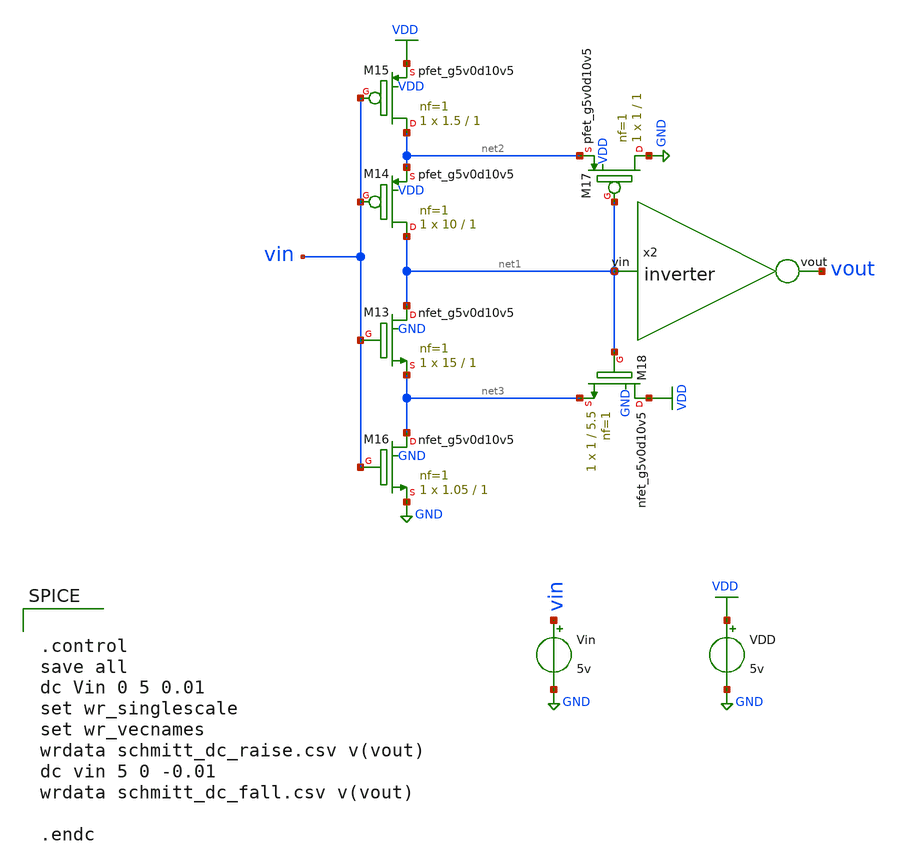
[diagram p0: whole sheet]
** sch_path: schematics/schmitt_trigger_tb.sch
**.subckt schmitt_trigger_tb
VDD VDD GND 5v
Vin vin GND 5v
XM13 net1 vin net3 GND sky130_fd_pr__nfet_g5v0d10v5 L=1 W=15 nf=1 ad='int((nf+1)/2) * W/nf * 0.29' as='int((nf+2)/2) * W/nf * 0.29'
+ pd='2*int((nf+1)/2) * (W/nf + 0.29)' ps='2*int((nf+2)/2) * (W/nf + 0.29)' nrd='0.29 / W' nrs='0.29 / W'
+ sa=0 sb=0 sd=0 mult=1 m=1
XM14 net1 vin net2 VDD sky130_fd_pr__pfet_g5v0d10v5 L=1 W=10 nf=1 ad='int((nf+1)/2) * W/nf * 0.29' as='int((nf+2)/2) * W/nf * 0.29'
+ pd='2*int((nf+1)/2) * (W/nf + 0.29)' ps='2*int((nf+2)/2) * (W/nf + 0.29)' nrd='0.29 / W' nrs='0.29 / W'
+ sa=0 sb=0 sd=0 mult=1 m=1
XM15 net2 vin VDD VDD sky130_fd_pr__pfet_g5v0d10v5 L=1 W=1.5 nf=1 ad='int((nf+1)/2) * W/nf * 0.29' as='int((nf+2)/2) * W/nf * 0.29'
+ pd='2*int((nf+1)/2) * (W/nf + 0.29)' ps='2*int((nf+2)/2) * (W/nf + 0.29)' nrd='0.29 / W' nrs='0.29 / W'
+ sa=0 sb=0 sd=0 mult=1 m=1
XM16 net3 vin GND GND sky130_fd_pr__nfet_g5v0d10v5 L=1 W=1.05 nf=1 ad='int((nf+1)/2) * W/nf * 0.29' as='int((nf+2)/2) * W/nf * 0.29'
+ pd='2*int((nf+1)/2) * (W/nf + 0.29)' ps='2*int((nf+2)/2) * (W/nf + 0.29)' nrd='0.29 / W' nrs='0.29 / W'
+ sa=0 sb=0 sd=0 mult=1 m=1
XM17 GND net1 net2 VDD sky130_fd_pr__pfet_g5v0d10v5 L=1 W=1 nf=1 ad='int((nf+1)/2) * W/nf * 0.29' as='int((nf+2)/2) * W/nf * 0.29'
+ pd='2*int((nf+1)/2) * (W/nf + 0.29)' ps='2*int((nf+2)/2) * (W/nf + 0.29)' nrd='0.29 / W' nrs='0.29 / W'
+ sa=0 sb=0 sd=0 mult=1 m=1
XM18 VDD net1 net3 GND sky130_fd_pr__nfet_g5v0d10v5 L=5.5 W=1 nf=1 ad='int((nf+1)/2) * W/nf * 0.29' as='int((nf+2)/2) * W/nf * 0.29'
+ pd='2*int((nf+1)/2) * (W/nf + 0.29)' ps='2*int((nf+2)/2) * (W/nf + 0.29)' nrd='0.29 / W' nrs='0.29 / W'
+ sa=0 sb=0 sd=0 mult=1 m=1
x2 vout net1 inverter
**** begin user architecture code


.control
save all
dc Vin 0 5 0.01
set wr_singlescale
set wr_vecnames
wrdata schmitt_dc_raise.csv v(vout)
dc vin 5 0 -0.01
wrdata schmitt_dc_fall.csv v(vout)

.endc


 .lib $::SKYWATER_MODELS/models/sky130.lib.spice tt

.param mc_mm_switch=0
.param mc_pr_switch=1

**** end user architecture code
**.ends

* expanding   symbol:  /media/sf_share/final_project/inverter.sym # of pins=2
** sym_path: schematics/inverter.sym
** sch_path: schematics/inverter.sch
.subckt inverter vout vin
*.ipin vin
*.opin vout
XM3 vout vin VDD VDD sky130_fd_pr__pfet_g5v0d10v5 L=0.5 W=0.5 nf=1 ad='int((nf+1)/2) * W/nf * 0.29' as='int((nf+2)/2) * W/nf * 0.29'
+ pd='2*int((nf+1)/2) * (W/nf + 0.29)' ps='2*int((nf+2)/2) * (W/nf + 0.29)' nrd='0.29 / W' nrs='0.29 / W'
+ sa=0 sb=0 sd=0 mult=1 m=1
XM5 vout vin GND GND sky130_fd_pr__nfet_g5v0d10v5 L=0.5 W=0.5 nf=1 ad='int((nf+1)/2) * W/nf * 0.29' as='int((nf+2)/2) * W/nf * 0.29'
+ pd='2*int((nf+1)/2) * (W/nf + 0.29)' ps='2*int((nf+2)/2) * (W/nf + 0.29)' nrd='0.29 / W' nrs='0.29 / W'
+ sa=0 sb=0 sd=0 mult=1 m=1
.ends

.GLOBAL VDD
.GLOBAL GND
.end
